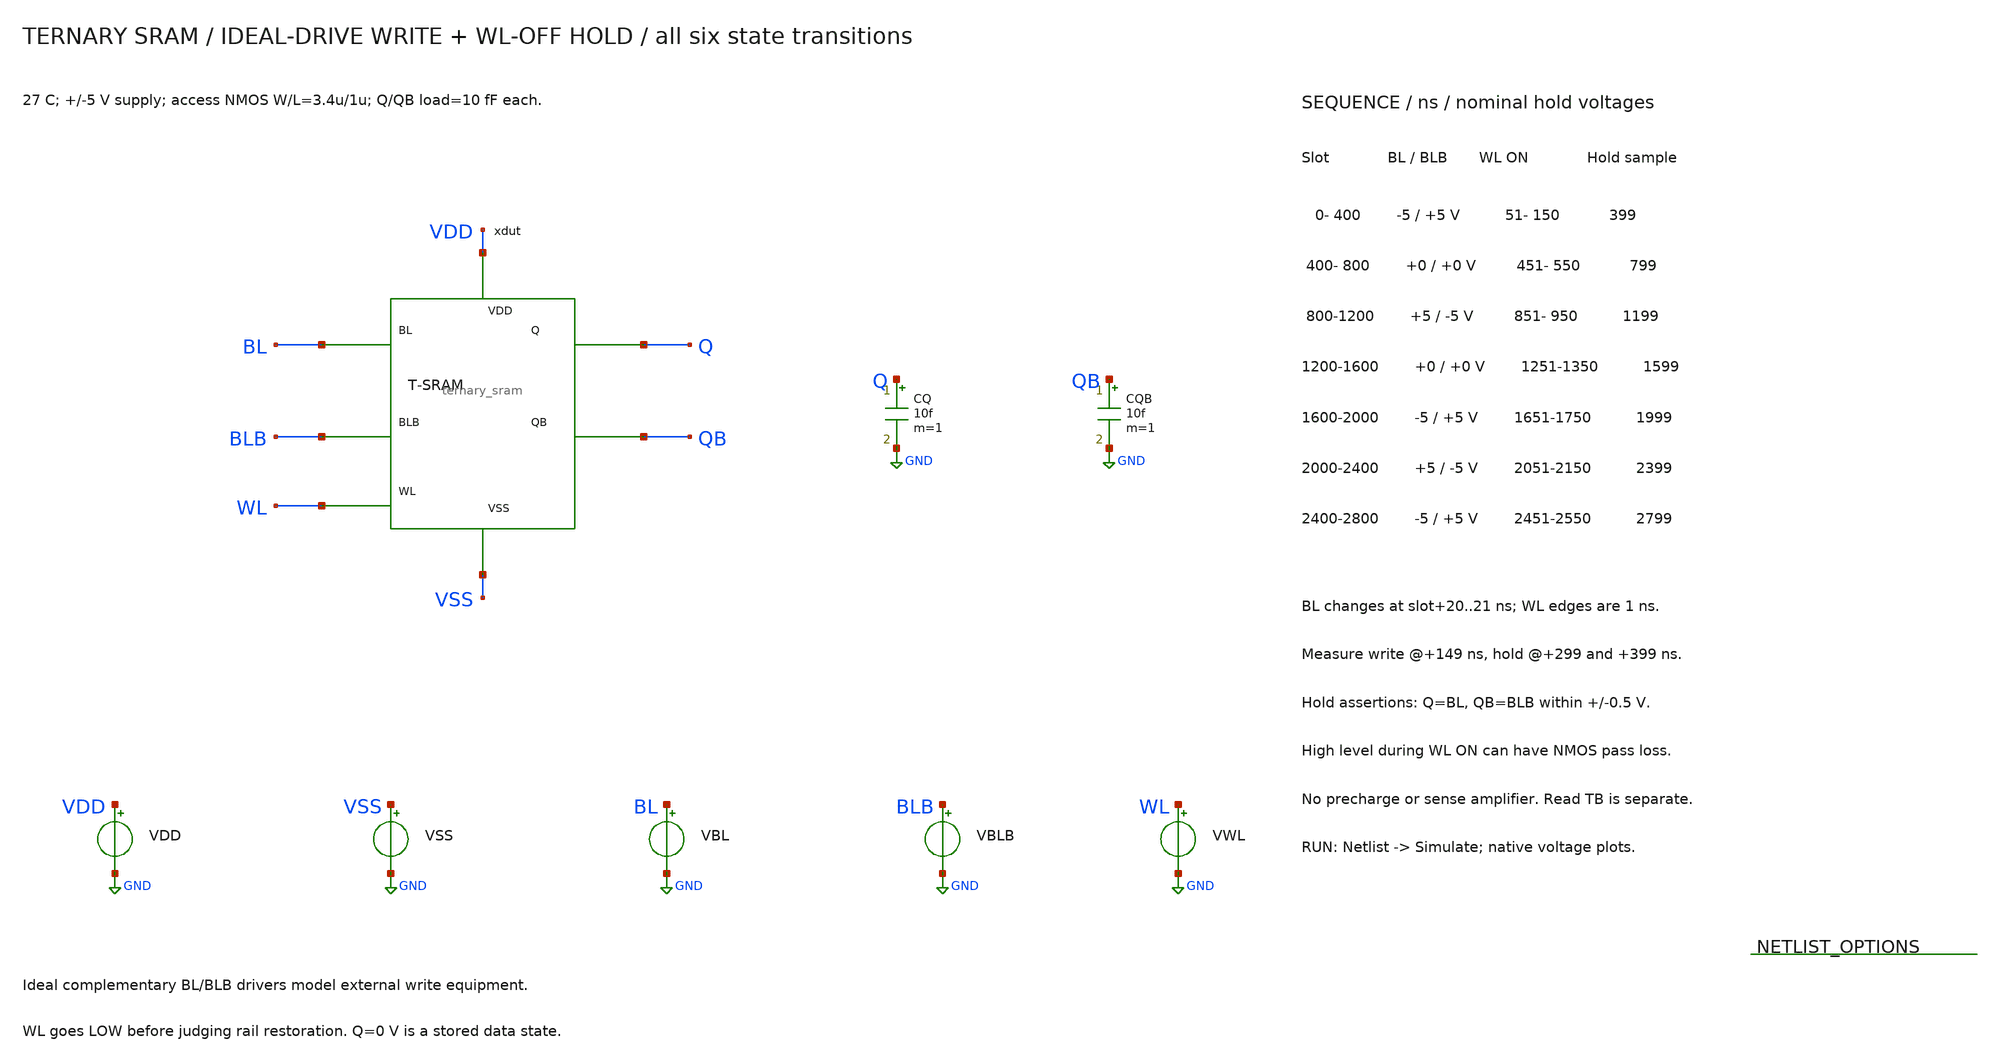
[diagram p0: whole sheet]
** sch_path: member_project/balanced-ternary-logic/PenguinEino/ternary_sram_tb.sch
**.subckt ternary_sram_tb
xdut BL BLB WL Q QB VDD VSS ternary_sram
CQ Q GND 10f m=1
CQB QB GND 10f m=1
VDD VDD GND 5
VSS VSS GND -5
VBL BL GND PWL(0n -5 420n -5 421n 0 820n 0 821n 5 1220n 5 1221n 0 1620n 0 1621n -5 2020n -5 2021n 5
+ 2420n 5 2421n -5 2800n -5)
VBLB BLB GND PWL(0n 5 420n 5 421n 0 820n 0 821n -5 1220n -5 1221n 0 1620n 0 1621n 5 2020n 5 2021n -5
+ 2420n -5 2421n 5 2800n 5)
VWL WL GND PWL(0n -5 50n -5 51n 5 150n 5 151n -5 450n -5 451n 5 550n 5 551n -5 850n -5 851n 5 950n 5
+ 951n -5 1250n -5 1251n 5 1350n 5 1351n -5 1650n -5 1651n 5 1750n 5 1751n -5 2050n -5 2051n 5 2150n 5
+ 2151n -5 2450n -5 2451n 5 2550n 5 2551n -5 2800n -5)
**** begin user architecture code
 .include $::LIB/ip62_models

.temp 27
.ic v(Q)=-5 v(QB)=5
.control
save all
set wr_singlescale
set wr_vecnames
setplot const
let failures=0
tran 0.2n 2800n 0 0.5n
meas tran write_q_0 find v(Q) at=149n
meas tran write_qb_0 find v(QB) at=149n
meas tran hold_q_299 find v(Q) at=299n
if abs(hold_q_299-(-5)) > 0.5
let const.failures=const.failures+1
echo FAIL: hold_q_299 expected -5 V
end
meas tran hold_qb_299 find v(QB) at=299n
if abs(hold_qb_299-(5)) > 0.5
let const.failures=const.failures+1
echo FAIL: hold_qb_299 expected 5 V
end
meas tran hold_q_399 find v(Q) at=399n
if abs(hold_q_399-(-5)) > 0.5
let const.failures=const.failures+1
echo FAIL: hold_q_399 expected -5 V
end
meas tran hold_qb_399 find v(QB) at=399n
if abs(hold_qb_399-(5)) > 0.5
let const.failures=const.failures+1
echo FAIL: hold_qb_399 expected 5 V
end
meas tran write_q_1 find v(Q) at=549n
meas tran write_qb_1 find v(QB) at=549n
meas tran hold_q_699 find v(Q) at=699n
if abs(hold_q_699-(0)) > 0.5
let const.failures=const.failures+1
echo FAIL: hold_q_699 expected 0 V
end
meas tran hold_qb_699 find v(QB) at=699n
if abs(hold_qb_699-(0)) > 0.5
let const.failures=const.failures+1
echo FAIL: hold_qb_699 expected 0 V
end
meas tran hold_q_799 find v(Q) at=799n
if abs(hold_q_799-(0)) > 0.5
let const.failures=const.failures+1
echo FAIL: hold_q_799 expected 0 V
end
meas tran hold_qb_799 find v(QB) at=799n
if abs(hold_qb_799-(0)) > 0.5
let const.failures=const.failures+1
echo FAIL: hold_qb_799 expected 0 V
end
meas tran write_q_2 find v(Q) at=949n
meas tran write_qb_2 find v(QB) at=949n
meas tran hold_q_1099 find v(Q) at=1099n
if abs(hold_q_1099-(5)) > 0.5
let const.failures=const.failures+1
echo FAIL: hold_q_1099 expected 5 V
end
meas tran hold_qb_1099 find v(QB) at=1099n
if abs(hold_qb_1099-(-5)) > 0.5
let const.failures=const.failures+1
echo FAIL: hold_qb_1099 expected -5 V
end
meas tran hold_q_1199 find v(Q) at=1199n
if abs(hold_q_1199-(5)) > 0.5
let const.failures=const.failures+1
echo FAIL: hold_q_1199 expected 5 V
end
meas tran hold_qb_1199 find v(QB) at=1199n
if abs(hold_qb_1199-(-5)) > 0.5
let const.failures=const.failures+1
echo FAIL: hold_qb_1199 expected -5 V
end
meas tran write_q_3 find v(Q) at=1349n
meas tran write_qb_3 find v(QB) at=1349n
meas tran hold_q_1499 find v(Q) at=1499n
if abs(hold_q_1499-(0)) > 0.5
let const.failures=const.failures+1
echo FAIL: hold_q_1499 expected 0 V
end
meas tran hold_qb_1499 find v(QB) at=1499n
if abs(hold_qb_1499-(0)) > 0.5
let const.failures=const.failures+1
echo FAIL: hold_qb_1499 expected 0 V
end
meas tran hold_q_1599 find v(Q) at=1599n
if abs(hold_q_1599-(0)) > 0.5
let const.failures=const.failures+1
echo FAIL: hold_q_1599 expected 0 V
end
meas tran hold_qb_1599 find v(QB) at=1599n
if abs(hold_qb_1599-(0)) > 0.5
let const.failures=const.failures+1
echo FAIL: hold_qb_1599 expected 0 V
end
meas tran write_q_4 find v(Q) at=1749n
meas tran write_qb_4 find v(QB) at=1749n
meas tran hold_q_1899 find v(Q) at=1899n
if abs(hold_q_1899-(-5)) > 0.5
let const.failures=const.failures+1
echo FAIL: hold_q_1899 expected -5 V
end
meas tran hold_qb_1899 find v(QB) at=1899n
if abs(hold_qb_1899-(5)) > 0.5
let const.failures=const.failures+1
echo FAIL: hold_qb_1899 expected 5 V
end
meas tran hold_q_1999 find v(Q) at=1999n
if abs(hold_q_1999-(-5)) > 0.5
let const.failures=const.failures+1
echo FAIL: hold_q_1999 expected -5 V
end
meas tran hold_qb_1999 find v(QB) at=1999n
if abs(hold_qb_1999-(5)) > 0.5
let const.failures=const.failures+1
echo FAIL: hold_qb_1999 expected 5 V
end
meas tran write_q_5 find v(Q) at=2149n
meas tran write_qb_5 find v(QB) at=2149n
meas tran hold_q_2299 find v(Q) at=2299n
if abs(hold_q_2299-(5)) > 0.5
let const.failures=const.failures+1
echo FAIL: hold_q_2299 expected 5 V
end
meas tran hold_qb_2299 find v(QB) at=2299n
if abs(hold_qb_2299-(-5)) > 0.5
let const.failures=const.failures+1
echo FAIL: hold_qb_2299 expected -5 V
end
meas tran hold_q_2399 find v(Q) at=2399n
if abs(hold_q_2399-(5)) > 0.5
let const.failures=const.failures+1
echo FAIL: hold_q_2399 expected 5 V
end
meas tran hold_qb_2399 find v(QB) at=2399n
if abs(hold_qb_2399-(-5)) > 0.5
let const.failures=const.failures+1
echo FAIL: hold_qb_2399 expected -5 V
end
meas tran write_q_6 find v(Q) at=2549n
meas tran write_qb_6 find v(QB) at=2549n
meas tran hold_q_2699 find v(Q) at=2699n
if abs(hold_q_2699-(-5)) > 0.5
let const.failures=const.failures+1
echo FAIL: hold_q_2699 expected -5 V
end
meas tran hold_qb_2699 find v(QB) at=2699n
if abs(hold_qb_2699-(5)) > 0.5
let const.failures=const.failures+1
echo FAIL: hold_qb_2699 expected 5 V
end
meas tran hold_q_2799 find v(Q) at=2799n
if abs(hold_q_2799-(-5)) > 0.5
let const.failures=const.failures+1
echo FAIL: hold_q_2799 expected -5 V
end
meas tran hold_qb_2799 find v(QB) at=2799n
if abs(hold_qb_2799-(5)) > 0.5
let const.failures=const.failures+1
echo FAIL: hold_qb_2799 expected 5 V
end
plot v(Q) v(QB) ylimit -5.5 5.5 title 'SRAM storage: write and hold'
plot v(BL) v(BLB) v(WL) ylimit -5.5 5.5 title 'SRAM ideal bitline drivers and WL'
wrdata ternary_sram_write.txt v(Q) v(QB) v(BL) v(BLB) v(WL)
if const.failures = 0
echo PASS: all six writes and WL-off hold
else
echo FAIL: all six writes and WL-off hold
end
print const.failures
.endc

**** end user architecture code
**.ends

* expanding   symbol:  /home/ishi-kai/balanced-ternary-logic/ternary_sram.sym # of pins=7
** sym_path: member_project/balanced-ternary-logic/PenguinEino/ternary_sram.sym
** sch_path: member_project/balanced-ternary-logic/PenguinEino/ternary_sram.sch
.subckt ternary_sram BL BLB WL Q QB VDD VSS
*.ipin WL
*.iopin BL
*.iopin BLB
*.opin Q
*.opin QB
*.iopin VDD
*.iopin VSS
x_store Q QB VDD VSS ternary_latch
XXM_A Q WL BL VSS NMOS w=3.4u l=1u nrd=0 nrs=0 m=1
XXM_AB QB WL BLB VSS NMOS w=3.4u l=1u nrd=0 nrs=0 m=1
.ends


* expanding   symbol:  /home/ishi-kai/balanced-ternary-logic/ternary_latch.sym # of pins=4
** sym_path: member_project/balanced-ternary-logic/PenguinEino/ternary_latch.sym
** sch_path: member_project/balanced-ternary-logic/PenguinEino/ternary_latch.sch
.subckt ternary_latch Q QB VDD VSS
*.opin Q
*.opin QB
*.iopin VDD
*.iopin VSS
x_q QB Q VDD VSS inverter
x_qb Q QB VDD VSS inverter
.ends


* expanding   symbol:  /home/ishi-kai/balanced-ternary-logic/inverter.sym # of pins=4
** sym_path: member_project/balanced-ternary-logic/PenguinEino/inverter.sym
** sch_path: member_project/balanced-ternary-logic/PenguinEino/inverter.sch
.subckt inverter vin vout VDD VSS
*.iopin VDD
*.ipin vin
*.opin vout
*.iopin VSS
XXM1 net1 vin VDD VDD PMOS w=13.5u l=1u nrd=0 nrs=0 m=1
XR1 net1 vout VDD F_RR w=2.8e-06 l=30e-06 R=1 tc1=0 tc2=0 m=1
XR2 vout net2 VDD F_RR w=2.8e-06 l=30e-06 R=1 tc1=0 tc2=0 m=1
XXM2 net2 vin VSS VSS NMOS w=5u l=1u nrd=0 nrs=0 m=1
.ends

.GLOBAL GND
.end
